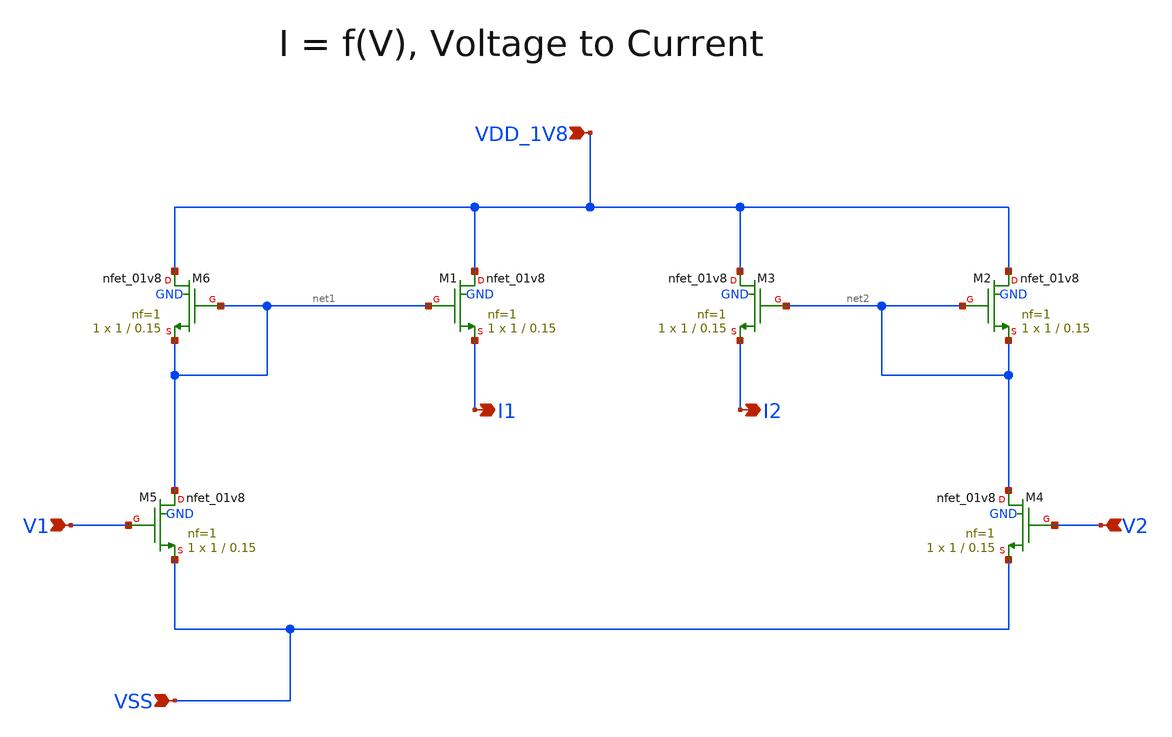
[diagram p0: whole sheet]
** sch_path: design/CNR_GR06_SKY130NM/CNR_GR06_V_to_I.sch
**.subckt CNR_GR06_V_to_I VDD_1V8 VSS I1 I2 V1 V2
*.ipin VDD_1V8
*.ipin VSS
*.opin I1
*.opin I2
*.ipin V1
*.ipin V2
XM6 VDD_1V8 net1 net1 GND sky130_fd_pr__nfet_01v8 L=0.15 W=1 nf=1 ad='int((nf+1)/2) * W/nf * 0.29' as='int((nf+2)/2) * W/nf * 0.29'
+ pd='2*int((nf+1)/2) * (W/nf + 0.29)' ps='2*int((nf+2)/2) * (W/nf + 0.29)' nrd='0.29 / W' nrs='0.29 / W'
+ sa=0 sb=0 sd=0 mult=1 m=1
XM1 VDD_1V8 net1 I1 GND sky130_fd_pr__nfet_01v8 L=0.15 W=1 nf=1 ad='int((nf+1)/2) * W/nf * 0.29' as='int((nf+2)/2) * W/nf * 0.29'
+ pd='2*int((nf+1)/2) * (W/nf + 0.29)' ps='2*int((nf+2)/2) * (W/nf + 0.29)' nrd='0.29 / W' nrs='0.29 / W'
+ sa=0 sb=0 sd=0 mult=1 m=1
XM2 VDD_1V8 net2 net2 GND sky130_fd_pr__nfet_01v8 L=0.15 W=1 nf=1 ad='int((nf+1)/2) * W/nf * 0.29' as='int((nf+2)/2) * W/nf * 0.29'
+ pd='2*int((nf+1)/2) * (W/nf + 0.29)' ps='2*int((nf+2)/2) * (W/nf + 0.29)' nrd='0.29 / W' nrs='0.29 / W'
+ sa=0 sb=0 sd=0 mult=1 m=1
XM3 VDD_1V8 net2 I2 GND sky130_fd_pr__nfet_01v8 L=0.15 W=1 nf=1 ad='int((nf+1)/2) * W/nf * 0.29' as='int((nf+2)/2) * W/nf * 0.29'
+ pd='2*int((nf+1)/2) * (W/nf + 0.29)' ps='2*int((nf+2)/2) * (W/nf + 0.29)' nrd='0.29 / W' nrs='0.29 / W'
+ sa=0 sb=0 sd=0 mult=1 m=1
XM4 net2 V2 VSS GND sky130_fd_pr__nfet_01v8 L=0.15 W=1 nf=1 ad='int((nf+1)/2) * W/nf * 0.29' as='int((nf+2)/2) * W/nf * 0.29'
+ pd='2*int((nf+1)/2) * (W/nf + 0.29)' ps='2*int((nf+2)/2) * (W/nf + 0.29)' nrd='0.29 / W' nrs='0.29 / W'
+ sa=0 sb=0 sd=0 mult=1 m=1
XM5 net1 V1 VSS GND sky130_fd_pr__nfet_01v8 L=0.15 W=1 nf=1 ad='int((nf+1)/2) * W/nf * 0.29' as='int((nf+2)/2) * W/nf * 0.29'
+ pd='2*int((nf+1)/2) * (W/nf + 0.29)' ps='2*int((nf+2)/2) * (W/nf + 0.29)' nrd='0.29 / W' nrs='0.29 / W'
+ sa=0 sb=0 sd=0 mult=1 m=1
**.ends
.end
